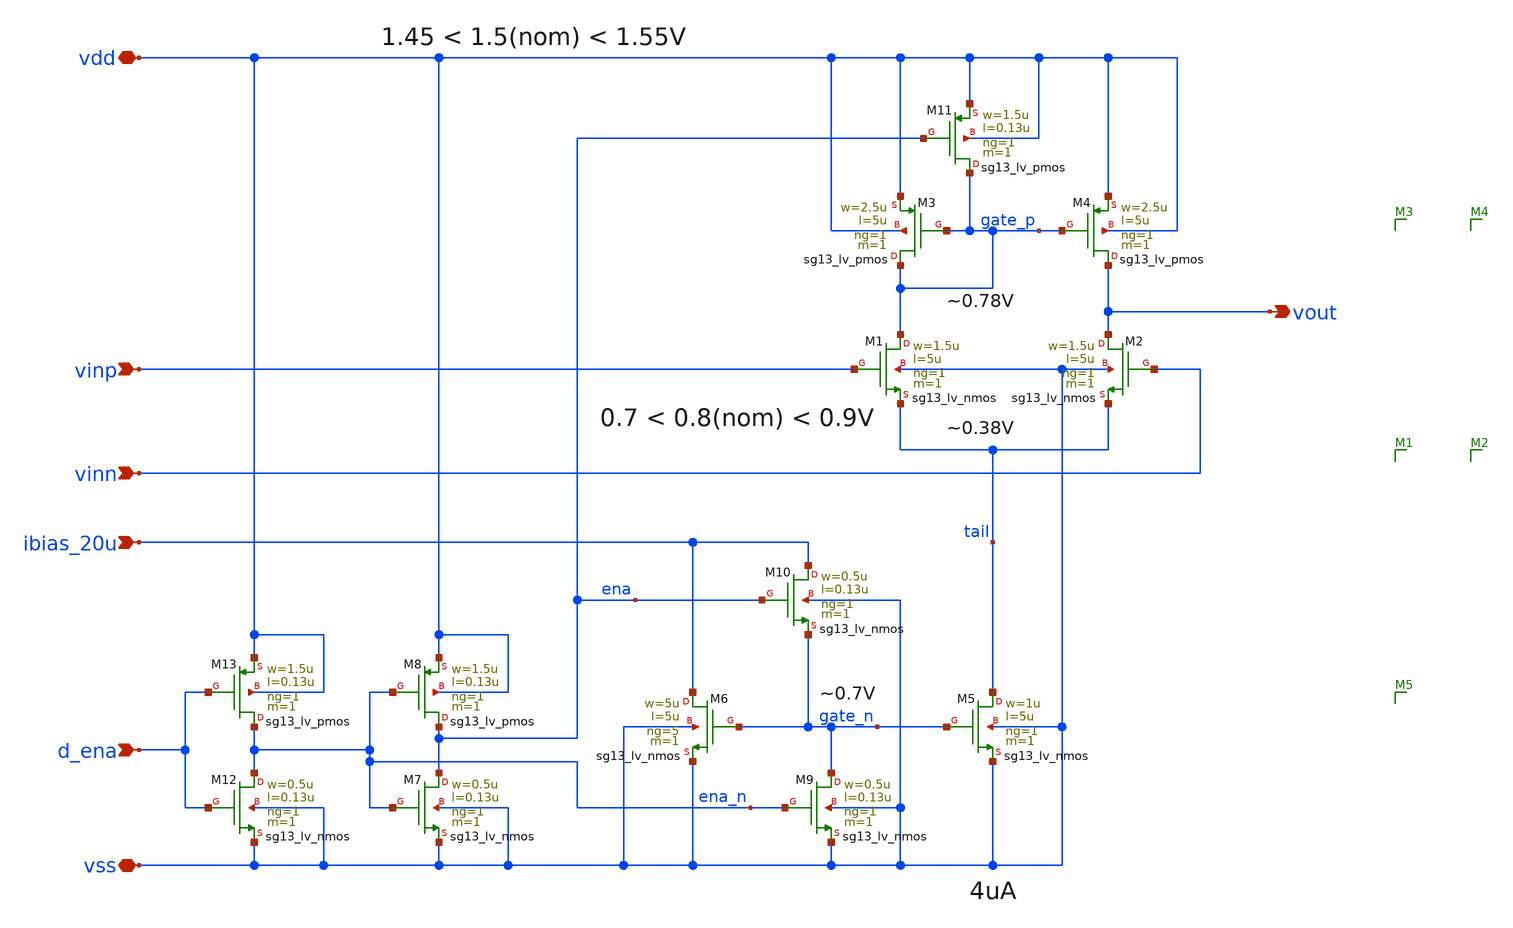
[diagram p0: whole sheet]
** sch_path: ota-5t-custom.sch
* (c) 2024-2025 Harald Pretl, Apache-2.0 license
**.subckt ota-5t-custom ibias_20u vdd vss vinp vinn vout d_ena
*.ipin ibias_20u
*.iopin vdd
*.iopin vss
*.ipin vinp
*.ipin vinn
*.opin vout
*.ipin d_ena
XM5 tail gate_n vss vss sg13_lv_nmos w=1u l=5u ng=1 m=1 mm_ok=1
XM4 vout gate_p vdd vdd sg13_lv_pmos w=2.5u l=5u ng=1 m=1 mm_ok=1
XM1 gate_p vinp tail vss sg13_lv_nmos w=1.5u l=5u ng=1 m=1 mm_ok=1
XM2 vout vinn tail vss sg13_lv_nmos w=1.5u l=5u ng=1 m=1 mm_ok=1
XM3 gate_p gate_p vdd vdd sg13_lv_pmos w=2.5u l=5u ng=1 m=1 mm_ok=1
XM6 ibias_20u gate_n vss vss sg13_lv_nmos w=5u l=5u ng=5 m=1 mm_ok=1
XM9 gate_n ena_n vss vss sg13_lv_nmos w=0.5u l=0.13u ng=1 m=1 mm_ok=1
XM11 gate_p ena vdd vdd sg13_lv_pmos w=1.5u l=0.13u ng=1 m=1 mm_ok=1
XM7 ena ena_n vss vss sg13_lv_nmos w=0.5u l=0.13u ng=1 m=1 mm_ok=1
XM8 ena ena_n vdd vdd sg13_lv_pmos w=1.5u l=0.13u ng=1 m=1 mm_ok=1
XM10 ibias_20u ena gate_n vss sg13_lv_nmos w=0.5u l=0.13u ng=1 m=1 mm_ok=1
XM12 ena_n d_ena vss vss sg13_lv_nmos w=0.5u l=0.13u ng=1 m=1 mm_ok=1
XM13 ena_n d_ena vdd vdd sg13_lv_pmos w=1.5u l=0.13u ng=1 m=1 mm_ok=1
**.ends
.end
